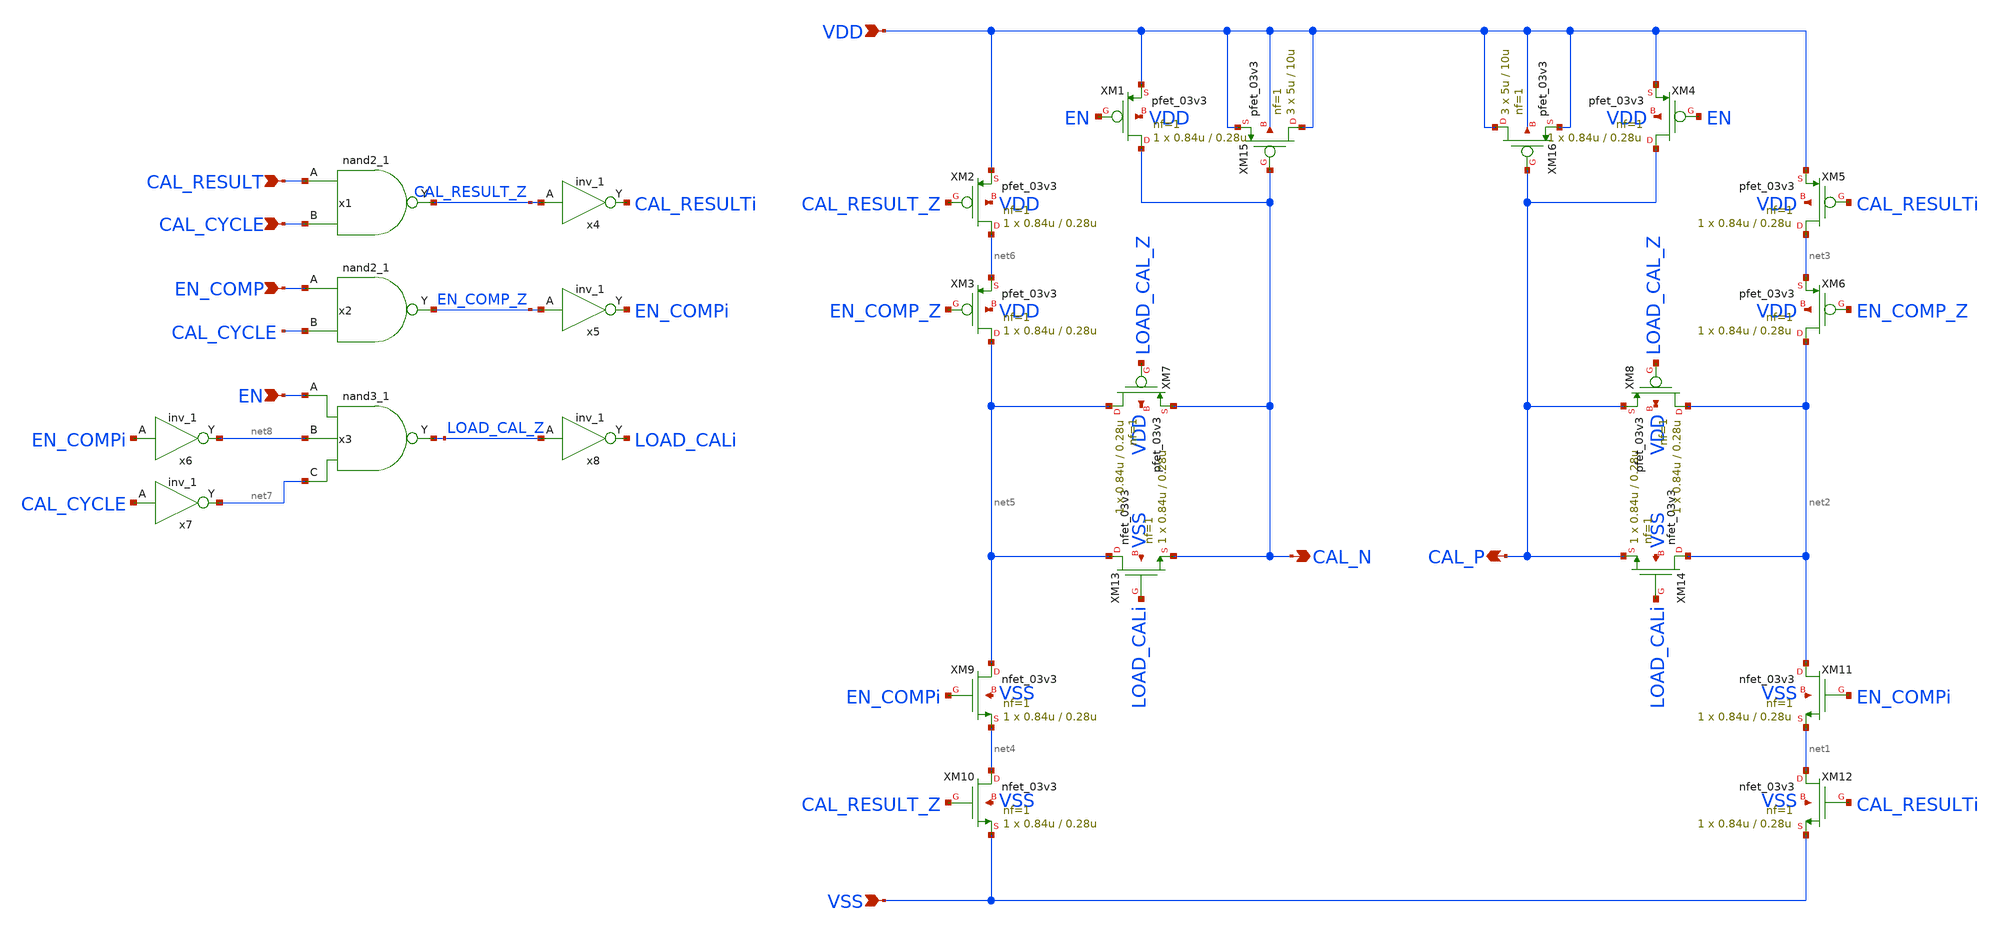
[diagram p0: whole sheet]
** sch_path: Schematic/offset_calibration/offset_calibration.sch
**.subckt offset_calibration EN_COMP CAL_N CAL_P VDD VSS EN CAL_RESULT CAL_CYCLE
*.ipin EN_COMP
*.opin CAL_N
*.opin CAL_P
*.ipin VDD
*.ipin VSS
*.ipin EN
*.ipin CAL_RESULT
*.ipin CAL_CYCLE
x1 CAL_RESULT CAL_CYCLE VGND VNB VPB VPWR CAL_RESULT_Z gf180mcu_fd_sc_mcu7t5v0__nand2_1
x2 EN_COMP CAL_CYCLE VGND VNB VPB VPWR EN_COMP_Z gf180mcu_fd_sc_mcu7t5v0__nand2_1
x4 CAL_RESULT_Z VGND VNB VPB VPWR CAL_RESULTi gf180mcu_fd_sc_mcu7t5v0__inv_1
x5 EN_COMP_Z VGND VNB VPB VPWR EN_COMPi gf180mcu_fd_sc_mcu7t5v0__inv_1
x6 EN_COMPi VGND VNB VPB VPWR net8 gf180mcu_fd_sc_mcu7t5v0__inv_1
x7 CAL_CYCLE VGND VNB VPB VPWR net7 gf180mcu_fd_sc_mcu7t5v0__inv_1
x3 EN net8 net7 VGND VNB VPB VPWR LOAD_CAL_Z gf180mcu_fd_sc_mcu7t5v0__nand3_1
x8 LOAD_CAL_Z VGND VNB VPB VPWR LOAD_CALi gf180mcu_fd_sc_mcu7t5v0__inv_1
XM1 CAL_N EN VDD VDD pfet_03v3 L=0.28u W=0.84u nf=1 ad='int((nf+1)/2) * W/nf * 0.18u' as='int((nf+2)/2) * W/nf * 0.18u'
+ pd='2*int((nf+1)/2) * (W/nf + 0.18u)' ps='2*int((nf+2)/2) * (W/nf + 0.18u)' nrd='0.18u / W' nrs='0.18u / W'
+ sa=0 sb=0 sd=0 m=1
XM9 net5 EN_COMPi net4 VSS nfet_03v3 L=0.28u W=0.84u nf=1 ad='int((nf+1)/2) * W/nf * 0.18u' as='int((nf+2)/2) * W/nf * 0.18u'
+ pd='2*int((nf+1)/2) * (W/nf + 0.18u)' ps='2*int((nf+2)/2) * (W/nf + 0.18u)' nrd='0.18u / W' nrs='0.18u / W'
+ sa=0 sb=0 sd=0 m=1
XM10 net4 CAL_RESULT_Z VSS VSS nfet_03v3 L=0.28u W=0.84u nf=1 ad='int((nf+1)/2) * W/nf * 0.18u' as='int((nf+2)/2) * W/nf * 0.18u'
+ pd='2*int((nf+1)/2) * (W/nf + 0.18u)' ps='2*int((nf+2)/2) * (W/nf + 0.18u)' nrd='0.18u / W' nrs='0.18u / W'
+ sa=0 sb=0 sd=0 m=1
XM11 net2 EN_COMPi net1 VSS nfet_03v3 L=0.28u W=0.84u nf=1 ad='int((nf+1)/2) * W/nf * 0.18u' as='int((nf+2)/2) * W/nf * 0.18u'
+ pd='2*int((nf+1)/2) * (W/nf + 0.18u)' ps='2*int((nf+2)/2) * (W/nf + 0.18u)' nrd='0.18u / W' nrs='0.18u / W'
+ sa=0 sb=0 sd=0 m=1
XM12 net1 CAL_RESULTi VSS VSS nfet_03v3 L=0.28u W=0.84u nf=1 ad='int((nf+1)/2) * W/nf * 0.18u' as='int((nf+2)/2) * W/nf * 0.18u'
+ pd='2*int((nf+1)/2) * (W/nf + 0.18u)' ps='2*int((nf+2)/2) * (W/nf + 0.18u)' nrd='0.18u / W' nrs='0.18u / W'
+ sa=0 sb=0 sd=0 m=1
XM13 net5 LOAD_CALi CAL_N VSS nfet_03v3 L=0.28u W=0.84u nf=1 ad='int((nf+1)/2) * W/nf * 0.18u' as='int((nf+2)/2) * W/nf * 0.18u'
+ pd='2*int((nf+1)/2) * (W/nf + 0.18u)' ps='2*int((nf+2)/2) * (W/nf + 0.18u)' nrd='0.18u / W' nrs='0.18u / W'
+ sa=0 sb=0 sd=0 m=1
XM14 net2 LOAD_CALi CAL_P VSS nfet_03v3 L=0.28u W=0.84u nf=1 ad='int((nf+1)/2) * W/nf * 0.18u' as='int((nf+2)/2) * W/nf * 0.18u'
+ pd='2*int((nf+1)/2) * (W/nf + 0.18u)' ps='2*int((nf+2)/2) * (W/nf + 0.18u)' nrd='0.18u / W' nrs='0.18u / W'
+ sa=0 sb=0 sd=0 m=1
XM15 VDD CAL_N VDD VDD pfet_03v3 L=10u W=5u nf=1 ad='int((nf+1)/2) * W/nf * 0.18u' as='int((nf+2)/2) * W/nf * 0.18u'
+ pd='2*int((nf+1)/2) * (W/nf + 0.18u)' ps='2*int((nf+2)/2) * (W/nf + 0.18u)' nrd='0.18u / W' nrs='0.18u / W'
+ sa=0 sb=0 sd=0 m=3
XM16 VDD CAL_P VDD VDD pfet_03v3 L=10u W=5u nf=1 ad='int((nf+1)/2) * W/nf * 0.18u' as='int((nf+2)/2) * W/nf * 0.18u'
+ pd='2*int((nf+1)/2) * (W/nf + 0.18u)' ps='2*int((nf+2)/2) * (W/nf + 0.18u)' nrd='0.18u / W' nrs='0.18u / W'
+ sa=0 sb=0 sd=0 m=3
XM2 net6 CAL_RESULT_Z VDD VDD pfet_03v3 L=0.28u W=0.84u nf=1 ad='int((nf+1)/2) * W/nf * 0.18u' as='int((nf+2)/2) * W/nf * 0.18u'
+ pd='2*int((nf+1)/2) * (W/nf + 0.18u)' ps='2*int((nf+2)/2) * (W/nf + 0.18u)' nrd='0.18u / W' nrs='0.18u / W'
+ sa=0 sb=0 sd=0 m=1
XM3 net5 EN_COMP_Z net6 VDD pfet_03v3 L=0.28u W=0.84u nf=1 ad='int((nf+1)/2) * W/nf * 0.18u' as='int((nf+2)/2) * W/nf * 0.18u'
+ pd='2*int((nf+1)/2) * (W/nf + 0.18u)' ps='2*int((nf+2)/2) * (W/nf + 0.18u)' nrd='0.18u / W' nrs='0.18u / W'
+ sa=0 sb=0 sd=0 m=1
XM4 CAL_P EN VDD VDD pfet_03v3 L=0.28u W=0.84u nf=1 ad='int((nf+1)/2) * W/nf * 0.18u' as='int((nf+2)/2) * W/nf * 0.18u'
+ pd='2*int((nf+1)/2) * (W/nf + 0.18u)' ps='2*int((nf+2)/2) * (W/nf + 0.18u)' nrd='0.18u / W' nrs='0.18u / W'
+ sa=0 sb=0 sd=0 m=1
XM5 net3 CAL_RESULTi VDD VDD pfet_03v3 L=0.28u W=0.84u nf=1 ad='int((nf+1)/2) * W/nf * 0.18u' as='int((nf+2)/2) * W/nf * 0.18u'
+ pd='2*int((nf+1)/2) * (W/nf + 0.18u)' ps='2*int((nf+2)/2) * (W/nf + 0.18u)' nrd='0.18u / W' nrs='0.18u / W'
+ sa=0 sb=0 sd=0 m=1
XM6 net2 EN_COMP_Z net3 VDD pfet_03v3 L=0.28u W=0.84u nf=1 ad='int((nf+1)/2) * W/nf * 0.18u' as='int((nf+2)/2) * W/nf * 0.18u'
+ pd='2*int((nf+1)/2) * (W/nf + 0.18u)' ps='2*int((nf+2)/2) * (W/nf + 0.18u)' nrd='0.18u / W' nrs='0.18u / W'
+ sa=0 sb=0 sd=0 m=1
XM7 net5 LOAD_CAL_Z CAL_N VDD pfet_03v3 L=0.28u W=0.84u nf=1 ad='int((nf+1)/2) * W/nf * 0.18u' as='int((nf+2)/2) * W/nf * 0.18u'
+ pd='2*int((nf+1)/2) * (W/nf + 0.18u)' ps='2*int((nf+2)/2) * (W/nf + 0.18u)' nrd='0.18u / W' nrs='0.18u / W'
+ sa=0 sb=0 sd=0 m=1
XM8 net2 LOAD_CAL_Z CAL_P VDD pfet_03v3 L=0.28u W=0.84u nf=1 ad='int((nf+1)/2) * W/nf * 0.18u' as='int((nf+2)/2) * W/nf * 0.18u'
+ pd='2*int((nf+1)/2) * (W/nf + 0.18u)' ps='2*int((nf+2)/2) * (W/nf + 0.18u)' nrd='0.18u / W' nrs='0.18u / W'
+ sa=0 sb=0 sd=0 m=1
**.ends
.end
